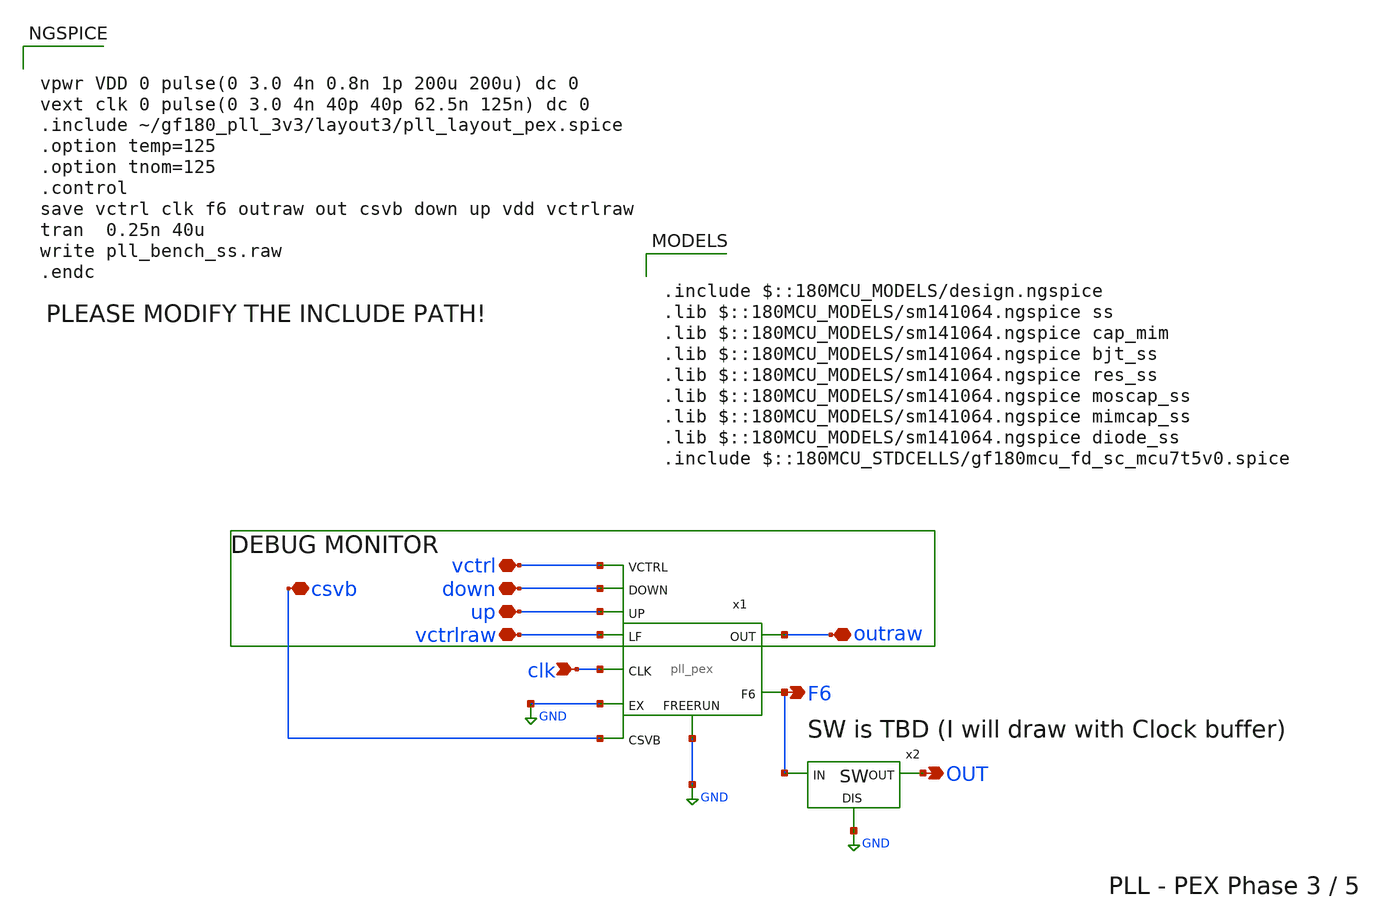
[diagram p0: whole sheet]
** sch_path: pex/pex_bench_ss.sch
**.subckt pex_bench_ss clk OUT F6 csvb up down vctrl vctrlraw outraw
*.ipin clk
*.opin OUT
*.opin F6
*.iopin csvb
*.iopin up
*.iopin down
*.iopin vctrl
*.iopin vctrlraw
*.iopin outraw
x1 up down vctrl clk VDD GND F6 0 outraw vctrlraw csvb GND TOP
x2 F6 OUT GND sw
**** begin user architecture code


vpwr VDD 0 pulse(0 3.0 4n 0.8n 1p 200u 200u) dc 0
vext clk 0 pulse(0 3.0 4n 40p 40p 62.5n 125n) dc 0
.include ~/gf180_pll_3v3/layout3/pll_layout_pex.spice
.option temp=125
.option tnom=125
.control
save vctrl clk f6 outraw out csvb down up vdd vctrlraw
tran  0.25n 40u
write pll_bench_ss.raw
.endc



.include $::180MCU_MODELS/design.ngspice
.lib $::180MCU_MODELS/sm141064.ngspice ss
.lib $::180MCU_MODELS/sm141064.ngspice cap_mim
.lib $::180MCU_MODELS/sm141064.ngspice bjt_ss
.lib $::180MCU_MODELS/sm141064.ngspice res_ss
.lib $::180MCU_MODELS/sm141064.ngspice moscap_ss
.lib $::180MCU_MODELS/sm141064.ngspice mimcap_ss
.lib $::180MCU_MODELS/sm141064.ngspice diode_ss
.include $::180MCU_STDCELLS/gf180mcu_fd_sc_mcu7t5v0.spice

**** end user architecture code
**.ends
.GLOBAL GND
.end
